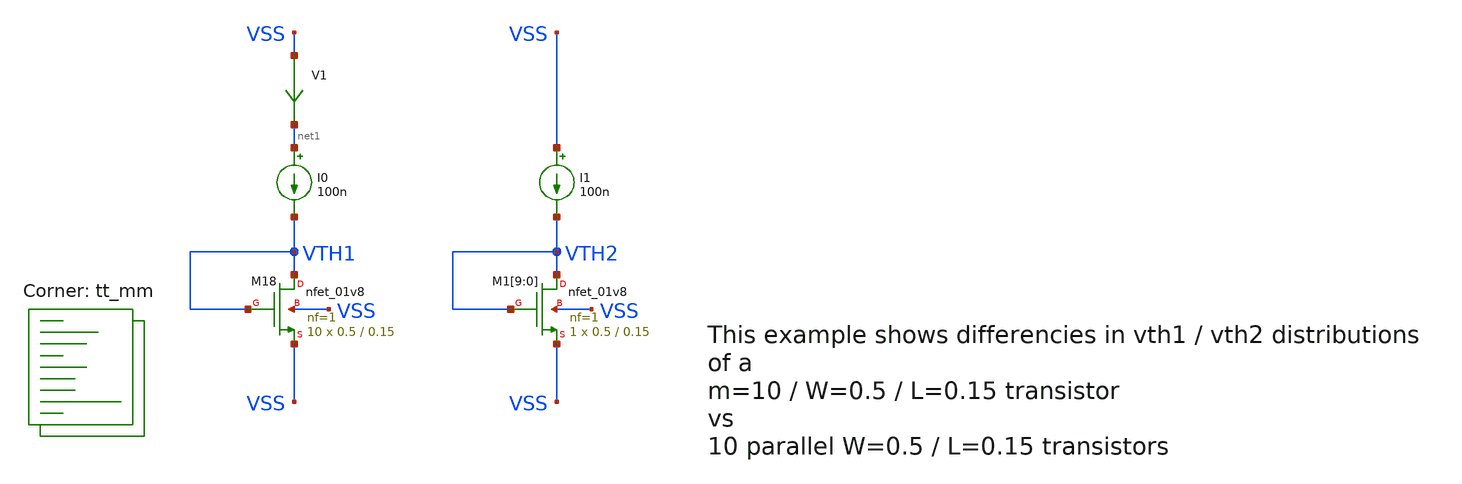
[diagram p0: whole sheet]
** sch_path: sky130A/xschem_libs/sky130_tests/sky130_mismatch/schematic/sky130_mismatch.sch
**.subckt sky130_mismatch
XM18 VTH1 VTH1 VSS VSS sky130_fd_pr__nfet_01v8 L=0.15 W=0.5 nf=1 ad='int((1 + 1)/2) * 0.5 / 1 * 0.29'
+ as='int((1 + 2)/2) * 0.5 / 1 * 0.29' pd='2*int((1 + 1)/2) * (0.5 / 1 + 0.29)' ps='2*int((1 + 2)/2) * (0.5 / 1 + 0.29)'
+ nrd='0.29 / 0.5 ' nrs='0.29 / 0.5 ' sa=0 sb=0 sd=0 mult=10 m=10
I0 net1 VTH1 100n
XM1[9] VTH2 VTH2 VSS VSS sky130_fd_pr__nfet_01v8 L=0.15 W=0.5 nf=1 ad='int((1 + 1)/2) * 0.5 / 1 * 0.29'
+ as='int((1 + 2)/2) * 0.5 / 1 * 0.29' pd='2*int((1 + 1)/2) * (0.5 / 1 + 0.29)' ps='2*int((1 + 2)/2) * (0.5 / 1 + 0.29)'
+ nrd='0.29 / 0.5 ' nrs='0.29 / 0.5 ' sa=0 sb=0 sd=0 mult=1 m=1
XM1[8] VTH2 VTH2 VSS VSS sky130_fd_pr__nfet_01v8 L=0.15 W=0.5 nf=1 ad='int((1 + 1)/2) * 0.5 / 1 * 0.29'
+ as='int((1 + 2)/2) * 0.5 / 1 * 0.29' pd='2*int((1 + 1)/2) * (0.5 / 1 + 0.29)' ps='2*int((1 + 2)/2) * (0.5 / 1 + 0.29)'
+ nrd='0.29 / 0.5 ' nrs='0.29 / 0.5 ' sa=0 sb=0 sd=0 mult=1 m=1
XM1[7] VTH2 VTH2 VSS VSS sky130_fd_pr__nfet_01v8 L=0.15 W=0.5 nf=1 ad='int((1 + 1)/2) * 0.5 / 1 * 0.29'
+ as='int((1 + 2)/2) * 0.5 / 1 * 0.29' pd='2*int((1 + 1)/2) * (0.5 / 1 + 0.29)' ps='2*int((1 + 2)/2) * (0.5 / 1 + 0.29)'
+ nrd='0.29 / 0.5 ' nrs='0.29 / 0.5 ' sa=0 sb=0 sd=0 mult=1 m=1
XM1[6] VTH2 VTH2 VSS VSS sky130_fd_pr__nfet_01v8 L=0.15 W=0.5 nf=1 ad='int((1 + 1)/2) * 0.5 / 1 * 0.29'
+ as='int((1 + 2)/2) * 0.5 / 1 * 0.29' pd='2*int((1 + 1)/2) * (0.5 / 1 + 0.29)' ps='2*int((1 + 2)/2) * (0.5 / 1 + 0.29)'
+ nrd='0.29 / 0.5 ' nrs='0.29 / 0.5 ' sa=0 sb=0 sd=0 mult=1 m=1
XM1[5] VTH2 VTH2 VSS VSS sky130_fd_pr__nfet_01v8 L=0.15 W=0.5 nf=1 ad='int((1 + 1)/2) * 0.5 / 1 * 0.29'
+ as='int((1 + 2)/2) * 0.5 / 1 * 0.29' pd='2*int((1 + 1)/2) * (0.5 / 1 + 0.29)' ps='2*int((1 + 2)/2) * (0.5 / 1 + 0.29)'
+ nrd='0.29 / 0.5 ' nrs='0.29 / 0.5 ' sa=0 sb=0 sd=0 mult=1 m=1
XM1[4] VTH2 VTH2 VSS VSS sky130_fd_pr__nfet_01v8 L=0.15 W=0.5 nf=1 ad='int((1 + 1)/2) * 0.5 / 1 * 0.29'
+ as='int((1 + 2)/2) * 0.5 / 1 * 0.29' pd='2*int((1 + 1)/2) * (0.5 / 1 + 0.29)' ps='2*int((1 + 2)/2) * (0.5 / 1 + 0.29)'
+ nrd='0.29 / 0.5 ' nrs='0.29 / 0.5 ' sa=0 sb=0 sd=0 mult=1 m=1
XM1[3] VTH2 VTH2 VSS VSS sky130_fd_pr__nfet_01v8 L=0.15 W=0.5 nf=1 ad='int((1 + 1)/2) * 0.5 / 1 * 0.29'
+ as='int((1 + 2)/2) * 0.5 / 1 * 0.29' pd='2*int((1 + 1)/2) * (0.5 / 1 + 0.29)' ps='2*int((1 + 2)/2) * (0.5 / 1 + 0.29)'
+ nrd='0.29 / 0.5 ' nrs='0.29 / 0.5 ' sa=0 sb=0 sd=0 mult=1 m=1
XM1[2] VTH2 VTH2 VSS VSS sky130_fd_pr__nfet_01v8 L=0.15 W=0.5 nf=1 ad='int((1 + 1)/2) * 0.5 / 1 * 0.29'
+ as='int((1 + 2)/2) * 0.5 / 1 * 0.29' pd='2*int((1 + 1)/2) * (0.5 / 1 + 0.29)' ps='2*int((1 + 2)/2) * (0.5 / 1 + 0.29)'
+ nrd='0.29 / 0.5 ' nrs='0.29 / 0.5 ' sa=0 sb=0 sd=0 mult=1 m=1
XM1[1] VTH2 VTH2 VSS VSS sky130_fd_pr__nfet_01v8 L=0.15 W=0.5 nf=1 ad='int((1 + 1)/2) * 0.5 / 1 * 0.29'
+ as='int((1 + 2)/2) * 0.5 / 1 * 0.29' pd='2*int((1 + 1)/2) * (0.5 / 1 + 0.29)' ps='2*int((1 + 2)/2) * (0.5 / 1 + 0.29)'
+ nrd='0.29 / 0.5 ' nrs='0.29 / 0.5 ' sa=0 sb=0 sd=0 mult=1 m=1
XM1[0] VTH2 VTH2 VSS VSS sky130_fd_pr__nfet_01v8 L=0.15 W=0.5 nf=1 ad='int((1 + 1)/2) * 0.5 / 1 * 0.29'
+ as='int((1 + 2)/2) * 0.5 / 1 * 0.29' pd='2*int((1 + 1)/2) * (0.5 / 1 + 0.29)' ps='2*int((1 + 2)/2) * (0.5 / 1 + 0.29)'
+ nrd='0.29 / 0.5 ' nrs='0.29 / 0.5 ' sa=0 sb=0 sd=0 mult=1 m=1
V1 VSS net1 0
.save i(v1)
I1 VSS VTH2 100n
**** begin user architecture code
.lib $::SKYWATER_MODELS/sky130.lib.spice tt_mm
**** end user architecture code
**.ends
**** begin user architecture code

* .option SCALE=1e-6
.option savecurrents
* this experimental option enables mos model bin
* selection based on W/NF instead of W
.option wnflag=1
.control
  setseed 12
  reset
  let run=0
  dowhile run < 1000
    save all
    op
    print run
    remzerovec
    write sky130_mismatch.raw
    set appendwrite
    let run = run + 1
    reset
  end
.endc


**** end user architecture code
.end
